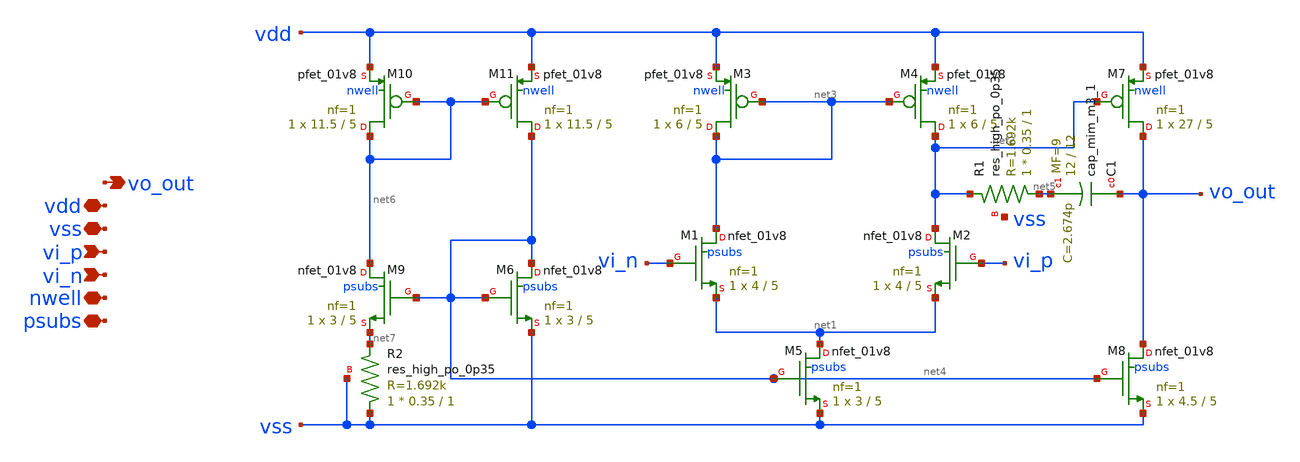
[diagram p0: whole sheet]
** sch_path: xschem/op.sch
**.subckt op vss vdd vo_out vi_p vi_n psubs nwell
*.iopin vss
*.iopin vdd
*.opin vo_out
*.ipin vi_p
*.ipin vi_n
*.iopin psubs
*.iopin nwell
XM1 net3 vi_n net1 psubs sky130_fd_pr__nfet_01v8 L=5 W=4 nf=1 ad='int((nf+1)/2) * W/nf * 0.29' as='int((nf+2)/2) * W/nf * 0.29'
+ pd='2*int((nf+1)/2) * (W/nf + 0.29)' ps='2*int((nf+2)/2) * (W/nf + 0.29)' nrd='0.29 / W' nrs='0.29 / W'
+ sa=0 sb=0 sd=0 mult=1 m=1
XM3 net3 net3 vdd nwell sky130_fd_pr__pfet_01v8 L=5 W=6 nf=1 ad='int((1 + 1)/2) * 6 / 1 * 0.29' as='int((1 + 2)/2) * 6 / 1 * 0.29'
+ pd='2*int((1 + 1)/2) * (6 / 1 + 0.29)' ps='2*int((1 + 2)/2) * (6 / 1 + 0.29)' nrd='0.29 / 6 ' nrs='0.29 / 6 '
+ sa=0 sb=0 sd=0 mult=1 m=1
XM6 net4 net4 vss psubs sky130_fd_pr__nfet_01v8 L=5 W=3 nf=1 ad='int((1 + 1)/2) * 3 / 1 * 0.29' as='int((1 + 2)/2) * 3 / 1 * 0.29'
+ pd='2*int((1 + 1)/2) * (3 / 1 + 0.29)' ps='2*int((1 + 2)/2) * (3 / 1 + 0.29)' nrd='0.29 / 3 ' nrs='0.29 / 3 '
+ sa=0 sb=0 sd=0 mult=1 m=1
XM5 net1 net4 vss psubs sky130_fd_pr__nfet_01v8 L=5 W=3 nf=1 ad='int((1 + 1)/2) * 3 / 1 * 0.29' as='int((1 + 2)/2) * 3 / 1 * 0.29'
+ pd='2*int((1 + 1)/2) * (3 / 1 + 0.29)' ps='2*int((1 + 2)/2) * (3 / 1 + 0.29)' nrd='0.29 / 3 ' nrs='0.29 / 3 '
+ sa=0 sb=0 sd=0 mult=1 m=1
XM7 vo_out net2 vdd nwell sky130_fd_pr__pfet_01v8 L=5 W=27 nf=1 ad='int((1 + 1)/2) * 27 / 1 * 0.29' as='int((1 + 2)/2) * 27 / 1 * 0.29'
+ pd='2*int((1 + 1)/2) * (27 / 1 + 0.29)' ps='2*int((1 + 2)/2) * (27 / 1 + 0.29)' nrd='0.29 / 27 ' nrs='0.29 / 27 '
+ sa=0 sb=0 sd=0 mult=1 m=1
XM8 vo_out net4 vss psubs sky130_fd_pr__nfet_01v8 L=5 W=4.5 nf=1 ad='int((1 + 1)/2) * 4.5 / 1 * 0.29'
+ as='int((1 + 2)/2) * 4.5 / 1 * 0.29' pd='2*int((1 + 1)/2) * (4.5 / 1 + 0.29)' ps='2*int((1 + 2)/2) * (4.5 / 1 + 0.29)'
+ nrd='0.29 / 4.5 ' nrs='0.29 / 4.5 ' sa=0 sb=0 sd=0 mult=1 m=1
XM2 net2 vi_p net1 psubs sky130_fd_pr__nfet_01v8 L=5 W=4 nf=1 ad='int((nf+1)/2) * W/nf * 0.29' as='int((nf+2)/2) * W/nf * 0.29'
+ pd='2*int((nf+1)/2) * (W/nf + 0.29)' ps='2*int((nf+2)/2) * (W/nf + 0.29)' nrd='0.29 / W' nrs='0.29 / W'
+ sa=0 sb=0 sd=0 mult=1 m=1
XM4 net2 net3 vdd nwell sky130_fd_pr__pfet_01v8 L=5 W=6 nf=1 ad='int((1 + 1)/2) * 6 / 1 * 0.29' as='int((1 + 2)/2) * 6 / 1 * 0.29'
+ pd='2*int((1 + 1)/2) * (6 / 1 + 0.29)' ps='2*int((1 + 2)/2) * (6 / 1 + 0.29)' nrd='0.29 / 6 ' nrs='0.29 / 6 '
+ sa=0 sb=0 sd=0 mult=1 m=1
XR1 net5 net2 vss sky130_fd_pr__res_high_po_0p35 L=1 mult=1 m=1
XC1 vo_out net5 sky130_fd_pr__cap_mim_m3_1 W=12 L=12 MF=9 m=9
XM9 net6 net4 net7 psubs sky130_fd_pr__nfet_01v8 L=5 W=3 nf=1 ad='int((1 + 1)/2) * 3 / 1 * 0.29' as='int((1 + 2)/2) * 3 / 1 * 0.29'
+ pd='2*int((1 + 1)/2) * (3 / 1 + 0.29)' ps='2*int((1 + 2)/2) * (3 / 1 + 0.29)' nrd='0.29 / 3 ' nrs='0.29 / 3 '
+ sa=0 sb=0 sd=0 mult=1 m=1
XM10 net6 net6 vdd nwell sky130_fd_pr__pfet_01v8 L=5 W=11.5 nf=1 ad='int((1 + 1)/2) * 11.5 / 1 * 0.29'
+ as='int((1 + 2)/2) * 11.5 / 1 * 0.29' pd='2*int((1 + 1)/2) * (11.5 / 1 + 0.29)' ps='2*int((1 + 2)/2) * (11.5 / 1 + 0.29)'
+ nrd='0.29 / 11.5 ' nrs='0.29 / 11.5 ' sa=0 sb=0 sd=0 mult=1 m=1
XM11 net4 net6 vdd nwell sky130_fd_pr__pfet_01v8 L=5 W=11.5 nf=1 ad='int((1 + 1)/2) * 11.5 / 1 * 0.29'
+ as='int((1 + 2)/2) * 11.5 / 1 * 0.29' pd='2*int((1 + 1)/2) * (11.5 / 1 + 0.29)' ps='2*int((1 + 2)/2) * (11.5 / 1 + 0.29)'
+ nrd='0.29 / 11.5 ' nrs='0.29 / 11.5 ' sa=0 sb=0 sd=0 mult=1 m=1
XR2 vss net7 vss sky130_fd_pr__res_high_po_0p35 L=1 mult=1 m=1
**.ends
.end
